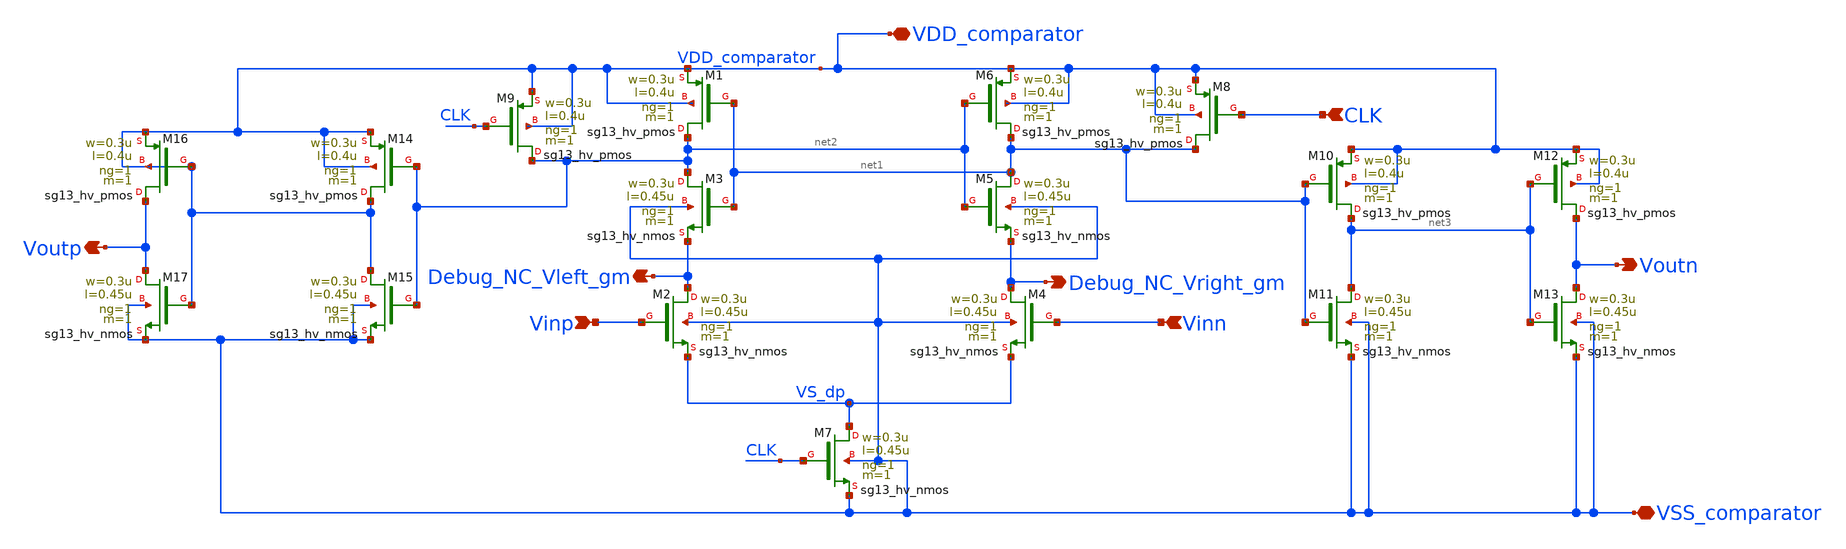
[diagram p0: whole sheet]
** sch_path: circuit_files/xschem_symbols/simple_comparator.sch
**.subckt simple_comparator CLK Vinp VSS_comparator VDD_comparator Vinn Debug_NC_Vright_gm
*+ Debug_NC_Vleft_gm Voutp Voutn
*.ipin CLK
*.ipin Vinp
*.iopin VSS_comparator
*.iopin VDD_comparator
*.ipin Vinn
*.opin Debug_NC_Vright_gm
*.opin Debug_NC_Vleft_gm
*.opin Voutp
*.opin Voutn
XM1 net2 net1 VDD_comparator VDD_comparator sg13_hv_pmos w=0.3u l=0.4u ng=1 m=1 mm_ok=1
XM2 Debug_NC_Vleft_gm Vinp VS_dp VSS_comparator sg13_hv_nmos w=0.3u l=0.45u ng=1 m=1 mm_ok=1
XM3 net2 net1 Debug_NC_Vleft_gm VSS_comparator sg13_hv_nmos w=0.3u l=0.45u ng=1 m=1 mm_ok=1
XM4 Debug_NC_Vright_gm Vinn VS_dp VSS_comparator sg13_hv_nmos w=0.3u l=0.45u ng=1 m=1 mm_ok=1
XM5 net1 net2 Debug_NC_Vright_gm VSS_comparator sg13_hv_nmos w=0.3u l=0.45u ng=1 m=1 mm_ok=1
XM6 net1 net2 VDD_comparator VDD_comparator sg13_hv_pmos w=0.3u l=0.4u ng=1 m=1 mm_ok=1
XM7 VS_dp CLK VSS_comparator VSS_comparator sg13_hv_nmos w=0.3u l=0.45u ng=1 m=1 mm_ok=1
XM8 net1 CLK VDD_comparator VDD_comparator sg13_hv_pmos w=0.3u l=0.4u ng=1 m=1 mm_ok=1
XM9 net2 CLK VDD_comparator VDD_comparator sg13_hv_pmos w=0.3u l=0.4u ng=1 m=1 mm_ok=1
XM10 net3 net1 VDD_comparator VDD_comparator sg13_hv_pmos w=0.3u l=0.4u ng=1 m=1 mm_ok=1
XM11 net3 net1 VSS_comparator VSS_comparator sg13_hv_nmos w=0.3u l=0.45u ng=1 m=1 mm_ok=1
XM12 Voutn net3 VDD_comparator VDD_comparator sg13_hv_pmos w=0.3u l=0.4u ng=1 m=1 mm_ok=1
XM13 Voutn net3 VSS_comparator VSS_comparator sg13_hv_nmos w=0.3u l=0.45u ng=1 m=1 mm_ok=1
XM14 VDD_comparator net2 VDD_comparator VDD_comparator sg13_hv_pmos w=0.3u l=0.4u ng=1 m=1 mm_ok=1
XM15 VDD_comparator net2 VSS_comparator VSS_comparator sg13_hv_nmos w=0.3u l=0.45u ng=1 m=1 mm_ok=1
XM16 Voutp VDD_comparator VDD_comparator VDD_comparator sg13_hv_pmos w=0.3u l=0.4u ng=1 m=1 mm_ok=1
XM17 Voutp VDD_comparator VSS_comparator VSS_comparator sg13_hv_nmos w=0.3u l=0.45u ng=1 m=1 mm_ok=1
**.ends
.end
